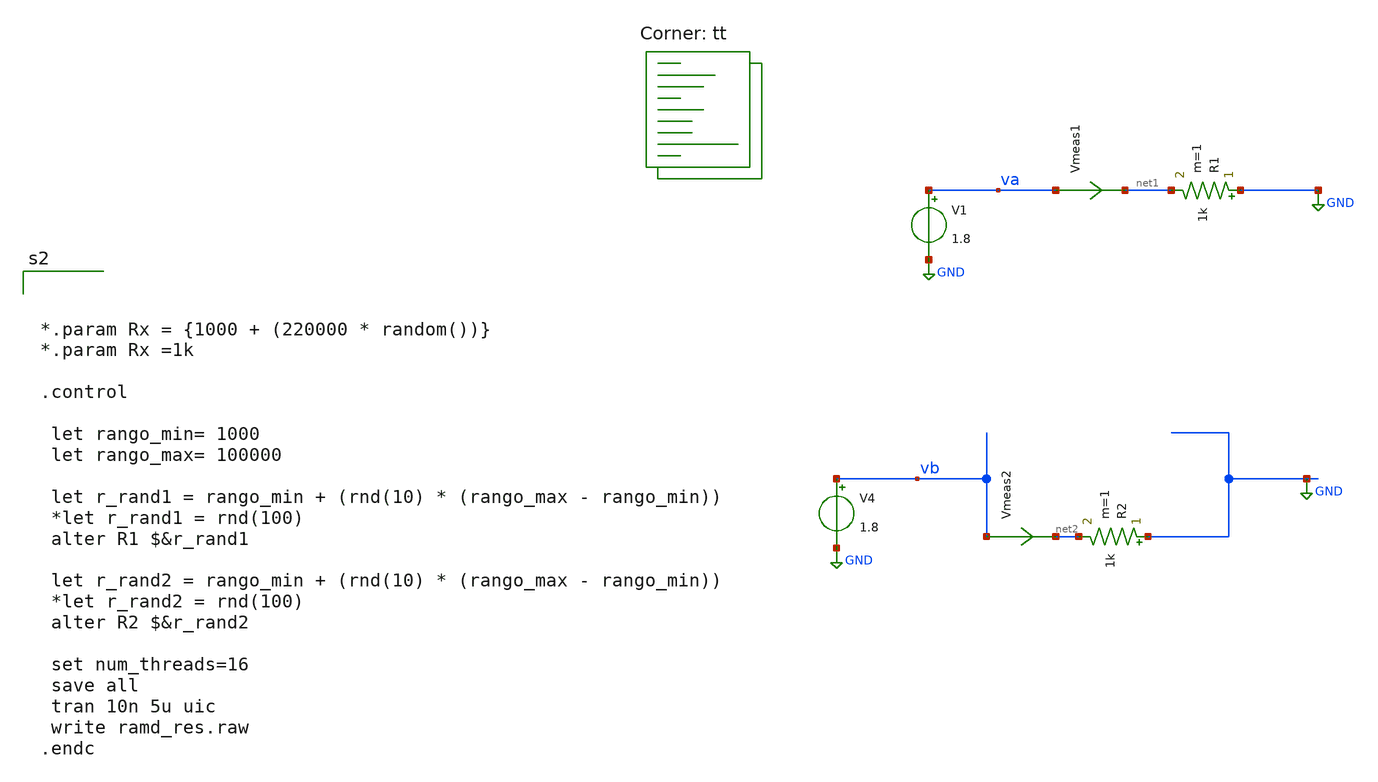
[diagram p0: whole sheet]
** sch_path: tests/ramd_res.sch
**.subckt ramd_res
V4 vb GND 1.8
R1 GND net1 1k m=1
R2 GND net2 1k m=1
V1 va GND 1.8
Vmeas1 va net1 0
.save i(vmeas1)
Vmeas2 vb net2 0
.save i(vmeas2)
**** begin user architecture code



*.param Rx = {1000 + (220000 * random())}
*.param Rx =1k

.control

 let rango_min= 1000
 let rango_max= 100000

 let r_rand1 = rango_min + (rnd(10) * (rango_max - rango_min))
 *let r_rand1 = rnd(100)
 alter R1 $&r_rand1

 let r_rand2 = rango_min + (rnd(10) * (rango_max - rango_min))
 *let r_rand2 = rnd(100)
 alter R2 $&r_rand2

 set num_threads=16
 save all
 tran 10n 5u uic
 write ramd_res.raw
.endc



.lib $::SKYWATER_MODELS/sky130.lib.spice tt

.subckt rram_cell BE TE gap_i=0.1
N1 BE TE rram_model
.model rram_model rram gap_initial={gap_i}
.ends rram_cell

.control
pre_osdi /foss/designs/spike_130/designs/prubs/rram.osdi
.endc

**** end user architecture code
**.ends
.GLOBAL GND
.end
